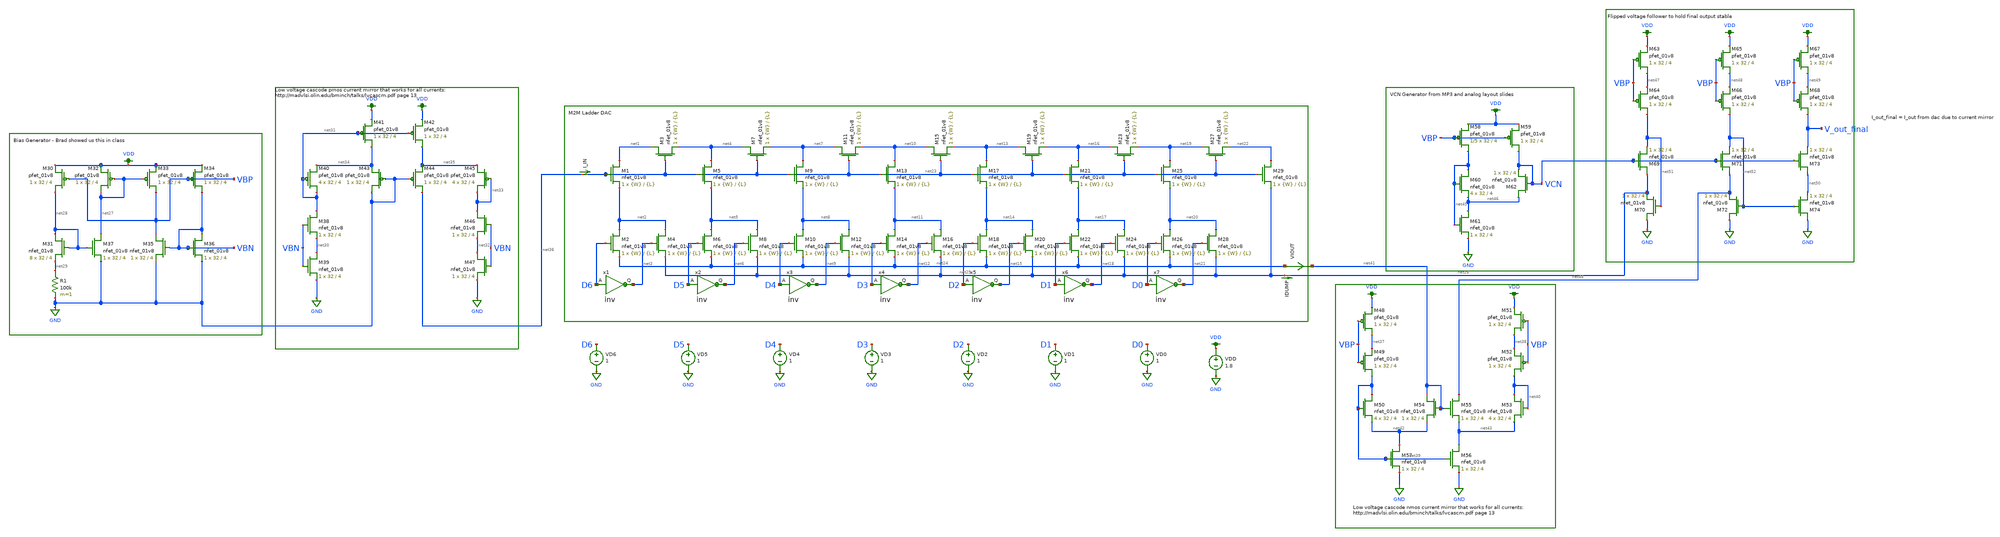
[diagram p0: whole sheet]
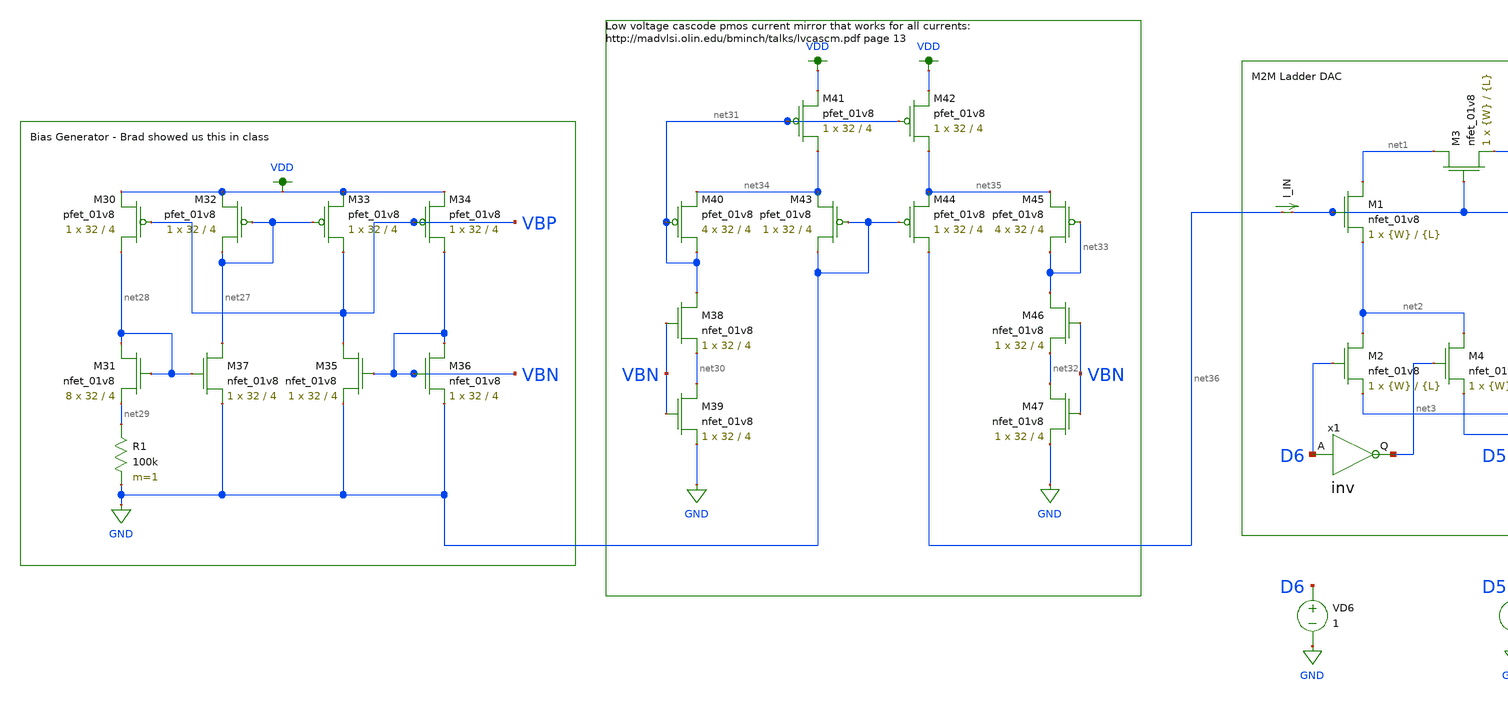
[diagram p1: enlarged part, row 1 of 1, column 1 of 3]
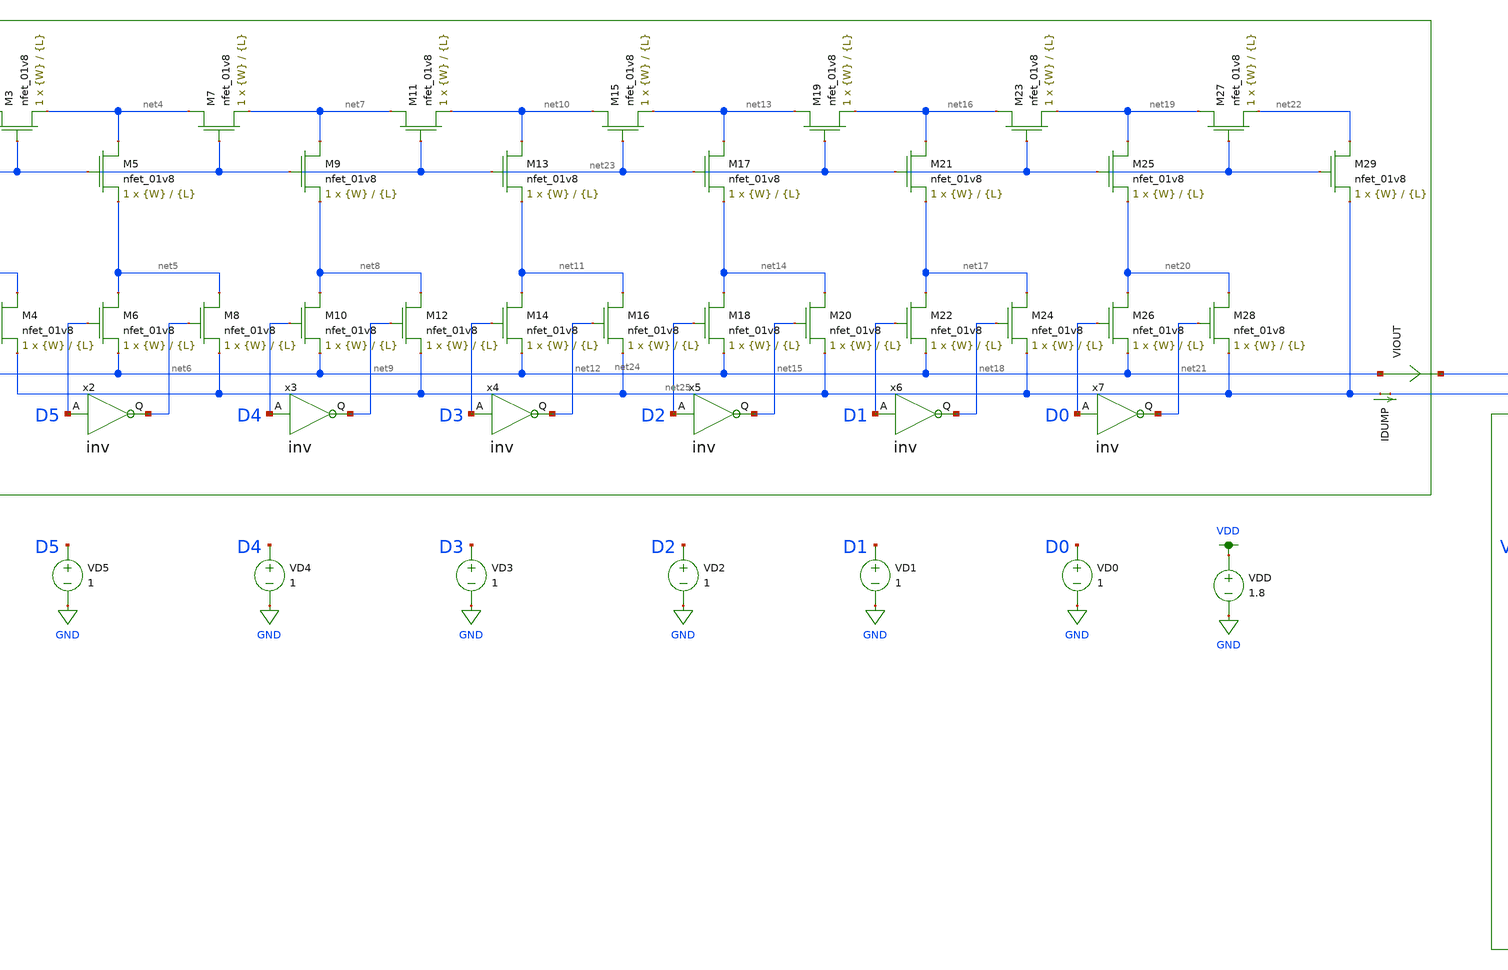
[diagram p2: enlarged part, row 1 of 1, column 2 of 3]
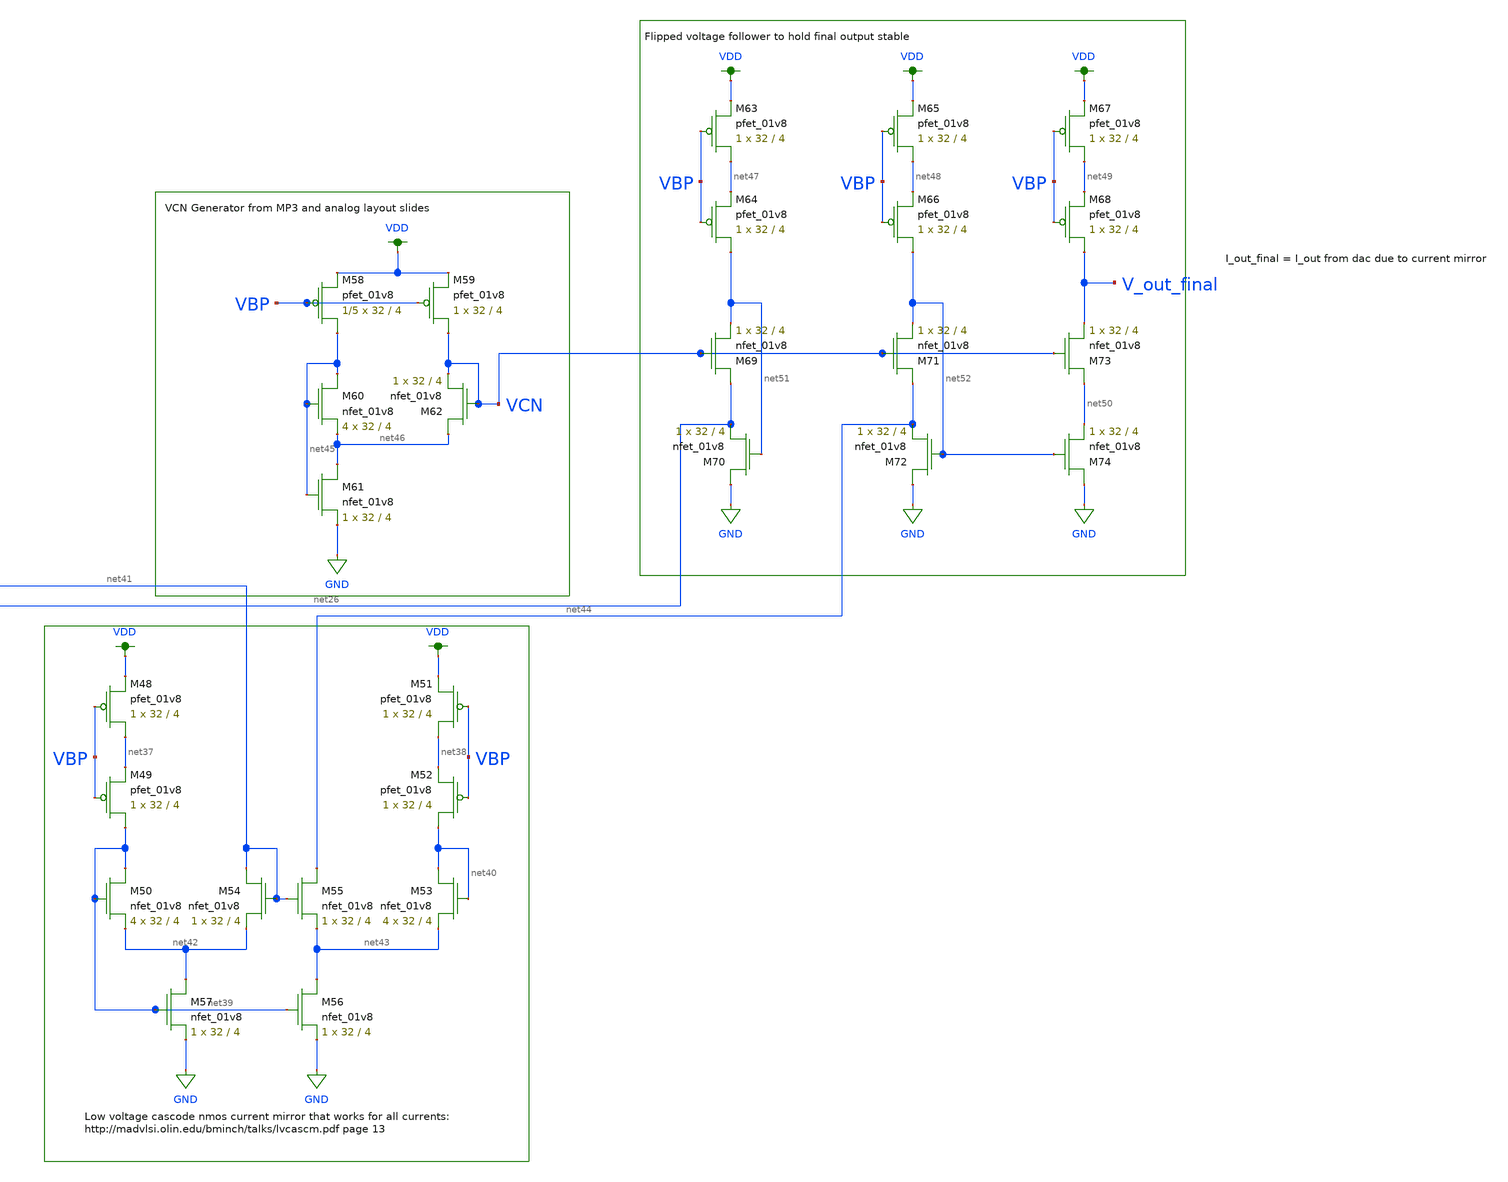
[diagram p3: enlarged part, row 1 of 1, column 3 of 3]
** sch_path: top_dac7.sch
**.subckt top_dac7
XM1 net1 net23 net2 GND sky130_fd_pr__nfet_01v8 L={L} W={W} nf=1 ad='int((nf+1)/2) * W/nf * 0.29' as='int((nf+2)/2) * W/nf * 0.29'
+ pd='2*int((nf+1)/2) * (W/nf + 0.29)' ps='2*int((nf+2)/2) * (W/nf + 0.29)' nrd='0.29 / W' nrs='0.29 / W'
+ sa=0 sb=0 sd=0 mult=1 m=1
XM2 net2 D6 net24 GND sky130_fd_pr__nfet_01v8 L={L} W={W} nf=1 ad='int((nf+1)/2) * W/nf * 0.29' as='int((nf+2)/2) * W/nf * 0.29'
+ pd='2*int((nf+1)/2) * (W/nf + 0.29)' ps='2*int((nf+2)/2) * (W/nf + 0.29)' nrd='0.29 / W' nrs='0.29 / W'
+ sa=0 sb=0 sd=0 mult=1 m=1
XM3 net1 net23 net4 GND sky130_fd_pr__nfet_01v8 L={L} W={W} nf=1 ad='int((nf+1)/2) * W/nf * 0.29' as='int((nf+2)/2) * W/nf * 0.29'
+ pd='2*int((nf+1)/2) * (W/nf + 0.29)' ps='2*int((nf+2)/2) * (W/nf + 0.29)' nrd='0.29 / W' nrs='0.29 / W'
+ sa=0 sb=0 sd=0 mult=1 m=1
XM4 net2 net3 net25 GND sky130_fd_pr__nfet_01v8 L={L} W={W} nf=1 ad='int((nf+1)/2) * W/nf * 0.29' as='int((nf+2)/2) * W/nf * 0.29'
+ pd='2*int((nf+1)/2) * (W/nf + 0.29)' ps='2*int((nf+2)/2) * (W/nf + 0.29)' nrd='0.29 / W' nrs='0.29 / W'
+ sa=0 sb=0 sd=0 mult=1 m=1
XM5 net4 net23 net5 GND sky130_fd_pr__nfet_01v8 L={L} W={W} nf=1 ad='int((nf+1)/2) * W/nf * 0.29' as='int((nf+2)/2) * W/nf * 0.29'
+ pd='2*int((nf+1)/2) * (W/nf + 0.29)' ps='2*int((nf+2)/2) * (W/nf + 0.29)' nrd='0.29 / W' nrs='0.29 / W'
+ sa=0 sb=0 sd=0 mult=1 m=1
XM6 net5 D5 net24 GND sky130_fd_pr__nfet_01v8 L={L} W={W} nf=1 ad='int((nf+1)/2) * W/nf * 0.29' as='int((nf+2)/2) * W/nf * 0.29'
+ pd='2*int((nf+1)/2) * (W/nf + 0.29)' ps='2*int((nf+2)/2) * (W/nf + 0.29)' nrd='0.29 / W' nrs='0.29 / W'
+ sa=0 sb=0 sd=0 mult=1 m=1
XM7 net4 net23 net7 GND sky130_fd_pr__nfet_01v8 L={L} W={W} nf=1 ad='int((nf+1)/2) * W/nf * 0.29' as='int((nf+2)/2) * W/nf * 0.29'
+ pd='2*int((nf+1)/2) * (W/nf + 0.29)' ps='2*int((nf+2)/2) * (W/nf + 0.29)' nrd='0.29 / W' nrs='0.29 / W'
+ sa=0 sb=0 sd=0 mult=1 m=1
XM8 net5 net6 net25 GND sky130_fd_pr__nfet_01v8 L={L} W={W} nf=1 ad='int((nf+1)/2) * W/nf * 0.29' as='int((nf+2)/2) * W/nf * 0.29'
+ pd='2*int((nf+1)/2) * (W/nf + 0.29)' ps='2*int((nf+2)/2) * (W/nf + 0.29)' nrd='0.29 / W' nrs='0.29 / W'
+ sa=0 sb=0 sd=0 mult=1 m=1
XM9 net7 net23 net8 GND sky130_fd_pr__nfet_01v8 L={L} W={W} nf=1 ad='int((nf+1)/2) * W/nf * 0.29' as='int((nf+2)/2) * W/nf * 0.29'
+ pd='2*int((nf+1)/2) * (W/nf + 0.29)' ps='2*int((nf+2)/2) * (W/nf + 0.29)' nrd='0.29 / W' nrs='0.29 / W'
+ sa=0 sb=0 sd=0 mult=1 m=1
XM10 net8 D4 net24 GND sky130_fd_pr__nfet_01v8 L={L} W={W} nf=1 ad='int((nf+1)/2) * W/nf * 0.29' as='int((nf+2)/2) * W/nf * 0.29'
+ pd='2*int((nf+1)/2) * (W/nf + 0.29)' ps='2*int((nf+2)/2) * (W/nf + 0.29)' nrd='0.29 / W' nrs='0.29 / W'
+ sa=0 sb=0 sd=0 mult=1 m=1
XM11 net7 net23 net10 GND sky130_fd_pr__nfet_01v8 L={L} W={W} nf=1 ad='int((nf+1)/2) * W/nf * 0.29' as='int((nf+2)/2) * W/nf * 0.29'
+ pd='2*int((nf+1)/2) * (W/nf + 0.29)' ps='2*int((nf+2)/2) * (W/nf + 0.29)' nrd='0.29 / W' nrs='0.29 / W'
+ sa=0 sb=0 sd=0 mult=1 m=1
XM12 net8 net9 net25 GND sky130_fd_pr__nfet_01v8 L={L} W={W} nf=1 ad='int((nf+1)/2) * W/nf * 0.29' as='int((nf+2)/2) * W/nf * 0.29'
+ pd='2*int((nf+1)/2) * (W/nf + 0.29)' ps='2*int((nf+2)/2) * (W/nf + 0.29)' nrd='0.29 / W' nrs='0.29 / W'
+ sa=0 sb=0 sd=0 mult=1 m=1
XM13 net10 net23 net11 GND sky130_fd_pr__nfet_01v8 L={L} W={W} nf=1 ad='int((nf+1)/2) * W/nf * 0.29'
+ as='int((nf+2)/2) * W/nf * 0.29' pd='2*int((nf+1)/2) * (W/nf + 0.29)' ps='2*int((nf+2)/2) * (W/nf + 0.29)'
+ nrd='0.29 / W' nrs='0.29 / W' sa=0 sb=0 sd=0 mult=1 m=1
XM14 net11 D3 net24 GND sky130_fd_pr__nfet_01v8 L={L} W={W} nf=1 ad='int((nf+1)/2) * W/nf * 0.29' as='int((nf+2)/2) * W/nf * 0.29'
+ pd='2*int((nf+1)/2) * (W/nf + 0.29)' ps='2*int((nf+2)/2) * (W/nf + 0.29)' nrd='0.29 / W' nrs='0.29 / W'
+ sa=0 sb=0 sd=0 mult=1 m=1
XM15 net10 net23 net13 GND sky130_fd_pr__nfet_01v8 L={L} W={W} nf=1 ad='int((nf+1)/2) * W/nf * 0.29'
+ as='int((nf+2)/2) * W/nf * 0.29' pd='2*int((nf+1)/2) * (W/nf + 0.29)' ps='2*int((nf+2)/2) * (W/nf + 0.29)'
+ nrd='0.29 / W' nrs='0.29 / W' sa=0 sb=0 sd=0 mult=1 m=1
XM16 net11 net12 net25 GND sky130_fd_pr__nfet_01v8 L={L} W={W} nf=1 ad='int((nf+1)/2) * W/nf * 0.29'
+ as='int((nf+2)/2) * W/nf * 0.29' pd='2*int((nf+1)/2) * (W/nf + 0.29)' ps='2*int((nf+2)/2) * (W/nf + 0.29)'
+ nrd='0.29 / W' nrs='0.29 / W' sa=0 sb=0 sd=0 mult=1 m=1
XM17 net13 net23 net14 GND sky130_fd_pr__nfet_01v8 L={L} W={W} nf=1 ad='int((nf+1)/2) * W/nf * 0.29'
+ as='int((nf+2)/2) * W/nf * 0.29' pd='2*int((nf+1)/2) * (W/nf + 0.29)' ps='2*int((nf+2)/2) * (W/nf + 0.29)'
+ nrd='0.29 / W' nrs='0.29 / W' sa=0 sb=0 sd=0 mult=1 m=1
XM18 net14 D2 net24 GND sky130_fd_pr__nfet_01v8 L={L} W={W} nf=1 ad='int((nf+1)/2) * W/nf * 0.29' as='int((nf+2)/2) * W/nf * 0.29'
+ pd='2*int((nf+1)/2) * (W/nf + 0.29)' ps='2*int((nf+2)/2) * (W/nf + 0.29)' nrd='0.29 / W' nrs='0.29 / W'
+ sa=0 sb=0 sd=0 mult=1 m=1
XM19 net13 net23 net16 GND sky130_fd_pr__nfet_01v8 L={L} W={W} nf=1 ad='int((nf+1)/2) * W/nf * 0.29'
+ as='int((nf+2)/2) * W/nf * 0.29' pd='2*int((nf+1)/2) * (W/nf + 0.29)' ps='2*int((nf+2)/2) * (W/nf + 0.29)'
+ nrd='0.29 / W' nrs='0.29 / W' sa=0 sb=0 sd=0 mult=1 m=1
XM20 net14 net15 net25 GND sky130_fd_pr__nfet_01v8 L={L} W={W} nf=1 ad='int((nf+1)/2) * W/nf * 0.29'
+ as='int((nf+2)/2) * W/nf * 0.29' pd='2*int((nf+1)/2) * (W/nf + 0.29)' ps='2*int((nf+2)/2) * (W/nf + 0.29)'
+ nrd='0.29 / W' nrs='0.29 / W' sa=0 sb=0 sd=0 mult=1 m=1
XM21 net16 net23 net17 GND sky130_fd_pr__nfet_01v8 L={L} W={W} nf=1 ad='int((nf+1)/2) * W/nf * 0.29'
+ as='int((nf+2)/2) * W/nf * 0.29' pd='2*int((nf+1)/2) * (W/nf + 0.29)' ps='2*int((nf+2)/2) * (W/nf + 0.29)'
+ nrd='0.29 / W' nrs='0.29 / W' sa=0 sb=0 sd=0 mult=1 m=1
XM22 net17 D1 net24 GND sky130_fd_pr__nfet_01v8 L={L} W={W} nf=1 ad='int((nf+1)/2) * W/nf * 0.29' as='int((nf+2)/2) * W/nf * 0.29'
+ pd='2*int((nf+1)/2) * (W/nf + 0.29)' ps='2*int((nf+2)/2) * (W/nf + 0.29)' nrd='0.29 / W' nrs='0.29 / W'
+ sa=0 sb=0 sd=0 mult=1 m=1
XM23 net16 net23 net19 GND sky130_fd_pr__nfet_01v8 L={L} W={W} nf=1 ad='int((nf+1)/2) * W/nf * 0.29'
+ as='int((nf+2)/2) * W/nf * 0.29' pd='2*int((nf+1)/2) * (W/nf + 0.29)' ps='2*int((nf+2)/2) * (W/nf + 0.29)'
+ nrd='0.29 / W' nrs='0.29 / W' sa=0 sb=0 sd=0 mult=1 m=1
XM24 net17 net18 net25 GND sky130_fd_pr__nfet_01v8 L={L} W={W} nf=1 ad='int((nf+1)/2) * W/nf * 0.29'
+ as='int((nf+2)/2) * W/nf * 0.29' pd='2*int((nf+1)/2) * (W/nf + 0.29)' ps='2*int((nf+2)/2) * (W/nf + 0.29)'
+ nrd='0.29 / W' nrs='0.29 / W' sa=0 sb=0 sd=0 mult=1 m=1
XM25 net19 net23 net20 GND sky130_fd_pr__nfet_01v8 L={L} W={W} nf=1 ad='int((nf+1)/2) * W/nf * 0.29'
+ as='int((nf+2)/2) * W/nf * 0.29' pd='2*int((nf+1)/2) * (W/nf + 0.29)' ps='2*int((nf+2)/2) * (W/nf + 0.29)'
+ nrd='0.29 / W' nrs='0.29 / W' sa=0 sb=0 sd=0 mult=1 m=1
XM26 net20 D0 net24 GND sky130_fd_pr__nfet_01v8 L={L} W={W} nf=1 ad='int((nf+1)/2) * W/nf * 0.29' as='int((nf+2)/2) * W/nf * 0.29'
+ pd='2*int((nf+1)/2) * (W/nf + 0.29)' ps='2*int((nf+2)/2) * (W/nf + 0.29)' nrd='0.29 / W' nrs='0.29 / W'
+ sa=0 sb=0 sd=0 mult=1 m=1
XM27 net19 net23 net22 GND sky130_fd_pr__nfet_01v8 L={L} W={W} nf=1 ad='int((nf+1)/2) * W/nf * 0.29'
+ as='int((nf+2)/2) * W/nf * 0.29' pd='2*int((nf+1)/2) * (W/nf + 0.29)' ps='2*int((nf+2)/2) * (W/nf + 0.29)'
+ nrd='0.29 / W' nrs='0.29 / W' sa=0 sb=0 sd=0 mult=1 m=1
XM28 net20 net21 net25 GND sky130_fd_pr__nfet_01v8 L={L} W={W} nf=1 ad='int((nf+1)/2) * W/nf * 0.29'
+ as='int((nf+2)/2) * W/nf * 0.29' pd='2*int((nf+1)/2) * (W/nf + 0.29)' ps='2*int((nf+2)/2) * (W/nf + 0.29)'
+ nrd='0.29 / W' nrs='0.29 / W' sa=0 sb=0 sd=0 mult=1 m=1
XM29 net22 net23 net25 GND sky130_fd_pr__nfet_01v8 L={L} W={W} nf=1 ad='int((nf+1)/2) * W/nf * 0.29'
+ as='int((nf+2)/2) * W/nf * 0.29' pd='2*int((nf+1)/2) * (W/nf + 0.29)' ps='2*int((nf+2)/2) * (W/nf + 0.29)'
+ nrd='0.29 / W' nrs='0.29 / W' sa=0 sb=0 sd=0 mult=1 m=1
IDUMP net25 net26 0
.save i(idump)
I_IN net36 net23 0
.save i(i_in)
x1 net3 D6 inv
x2 net6 D5 inv
x3 net9 D4 inv
x4 net12 D3 inv
x5 net15 D2 inv
x6 net18 D1 inv
x7 net21 D0 inv
XM30 net28 VBP VDD VDD sky130_fd_pr__pfet_01v8 L=4 W=32 nf=1 ad='int((nf+1)/2) * W/nf * 0.29' as='int((nf+2)/2) * W/nf * 0.29'
+ pd='2*int((nf+1)/2) * (W/nf + 0.29)' ps='2*int((nf+2)/2) * (W/nf + 0.29)' nrd='0.29 / W' nrs='0.29 / W'
+ sa=0 sb=0 sd=0 mult=1 m=1
XM31 net28 net28 net29 GND sky130_fd_pr__nfet_01v8 L=4 W=32 nf=1 ad='int((nf+1)/2) * W/nf * 0.29' as='int((nf+2)/2) * W/nf * 0.29'
+ pd='2*int((nf+1)/2) * (W/nf + 0.29)' ps='2*int((nf+2)/2) * (W/nf + 0.29)' nrd='0.29 / W' nrs='0.29 / W'
+ sa=0 sb=0 sd=0 mult=8 m=8
XM32 net27 net27 VDD VDD sky130_fd_pr__pfet_01v8 L=4 W=32 nf=1 ad='int((nf+1)/2) * W/nf * 0.29' as='int((nf+2)/2) * W/nf * 0.29'
+ pd='2*int((nf+1)/2) * (W/nf + 0.29)' ps='2*int((nf+2)/2) * (W/nf + 0.29)' nrd='0.29 / W' nrs='0.29 / W'
+ sa=0 sb=0 sd=0 mult=1 m=1
XM33 VBP net27 VDD VDD sky130_fd_pr__pfet_01v8 L=4 W=32 nf=1 ad='int((nf+1)/2) * W/nf * 0.29' as='int((nf+2)/2) * W/nf * 0.29'
+ pd='2*int((nf+1)/2) * (W/nf + 0.29)' ps='2*int((nf+2)/2) * (W/nf + 0.29)' nrd='0.29 / W' nrs='0.29 / W'
+ sa=0 sb=0 sd=0 mult=1 m=1
XM34 VBN VBP VDD VDD sky130_fd_pr__pfet_01v8 L=4 W=32 nf=1 ad='int((nf+1)/2) * W/nf * 0.29' as='int((nf+2)/2) * W/nf * 0.29'
+ pd='2*int((nf+1)/2) * (W/nf + 0.29)' ps='2*int((nf+2)/2) * (W/nf + 0.29)' nrd='0.29 / W' nrs='0.29 / W'
+ sa=0 sb=0 sd=0 mult=1 m=1
XM35 VBP VBN GND GND sky130_fd_pr__nfet_01v8 L=4 W=32 nf=1 ad='int((nf+1)/2) * W/nf * 0.29' as='int((nf+2)/2) * W/nf * 0.29'
+ pd='2*int((nf+1)/2) * (W/nf + 0.29)' ps='2*int((nf+2)/2) * (W/nf + 0.29)' nrd='0.29 / W' nrs='0.29 / W'
+ sa=0 sb=0 sd=0 mult=1 m=1
XM36 VBN VBN GND GND sky130_fd_pr__nfet_01v8 L=4 W=32 nf=1 ad='int((nf+1)/2) * W/nf * 0.29' as='int((nf+2)/2) * W/nf * 0.29'
+ pd='2*int((nf+1)/2) * (W/nf + 0.29)' ps='2*int((nf+2)/2) * (W/nf + 0.29)' nrd='0.29 / W' nrs='0.29 / W'
+ sa=0 sb=0 sd=0 mult=1 m=1
XM37 net27 net28 GND GND sky130_fd_pr__nfet_01v8 L=4 W=32 nf=1 ad='int((nf+1)/2) * W/nf * 0.29' as='int((nf+2)/2) * W/nf * 0.29'
+ pd='2*int((nf+1)/2) * (W/nf + 0.29)' ps='2*int((nf+2)/2) * (W/nf + 0.29)' nrd='0.29 / W' nrs='0.29 / W'
+ sa=0 sb=0 sd=0 mult=1 m=1
R1 net29 GND 100k m=1
XM38 net31 VBN net30 GND sky130_fd_pr__nfet_01v8 L=4 W=32 nf=1 ad='int((nf+1)/2) * W/nf * 0.29' as='int((nf+2)/2) * W/nf * 0.29'
+ pd='2*int((nf+1)/2) * (W/nf + 0.29)' ps='2*int((nf+2)/2) * (W/nf + 0.29)' nrd='0.29 / W' nrs='0.29 / W'
+ sa=0 sb=0 sd=0 mult=1 m=1
XM39 net30 VBN GND GND sky130_fd_pr__nfet_01v8 L=4 W=32 nf=1 ad='int((nf+1)/2) * W/nf * 0.29' as='int((nf+2)/2) * W/nf * 0.29'
+ pd='2*int((nf+1)/2) * (W/nf + 0.29)' ps='2*int((nf+2)/2) * (W/nf + 0.29)' nrd='0.29 / W' nrs='0.29 / W'
+ sa=0 sb=0 sd=0 mult=1 m=1
XM40 net31 net31 net34 VDD sky130_fd_pr__pfet_01v8 L=4 W=32 nf=1 ad='int((nf+1)/2) * W/nf * 0.29' as='int((nf+2)/2) * W/nf * 0.29'
+ pd='2*int((nf+1)/2) * (W/nf + 0.29)' ps='2*int((nf+2)/2) * (W/nf + 0.29)' nrd='0.29 / W' nrs='0.29 / W'
+ sa=0 sb=0 sd=0 mult=4 m=4
XM41 net34 net31 VDD VDD sky130_fd_pr__pfet_01v8 L=4 W=32 nf=1 ad='int((nf+1)/2) * W/nf * 0.29' as='int((nf+2)/2) * W/nf * 0.29'
+ pd='2*int((nf+1)/2) * (W/nf + 0.29)' ps='2*int((nf+2)/2) * (W/nf + 0.29)' nrd='0.29 / W' nrs='0.29 / W'
+ sa=0 sb=0 sd=0 mult=1 m=1
XM42 net35 net31 VDD VDD sky130_fd_pr__pfet_01v8 L=4 W=32 nf=1 ad='int((nf+1)/2) * W/nf * 0.29' as='int((nf+2)/2) * W/nf * 0.29'
+ pd='2*int((nf+1)/2) * (W/nf + 0.29)' ps='2*int((nf+2)/2) * (W/nf + 0.29)' nrd='0.29 / W' nrs='0.29 / W'
+ sa=0 sb=0 sd=0 mult=1 m=1
XM43 GND GND net34 VDD sky130_fd_pr__pfet_01v8 L=4 W=32 nf=1 ad='int((nf+1)/2) * W/nf * 0.29' as='int((nf+2)/2) * W/nf * 0.29'
+ pd='2*int((nf+1)/2) * (W/nf + 0.29)' ps='2*int((nf+2)/2) * (W/nf + 0.29)' nrd='0.29 / W' nrs='0.29 / W'
+ sa=0 sb=0 sd=0 mult=1 m=1
XM44 net36 GND net35 VDD sky130_fd_pr__pfet_01v8 L=4 W=32 nf=1 ad='int((nf+1)/2) * W/nf * 0.29' as='int((nf+2)/2) * W/nf * 0.29'
+ pd='2*int((nf+1)/2) * (W/nf + 0.29)' ps='2*int((nf+2)/2) * (W/nf + 0.29)' nrd='0.29 / W' nrs='0.29 / W'
+ sa=0 sb=0 sd=0 mult=1 m=1
XM45 net33 net33 net35 VDD sky130_fd_pr__pfet_01v8 L=4 W=32 nf=1 ad='int((nf+1)/2) * W/nf * 0.29' as='int((nf+2)/2) * W/nf * 0.29'
+ pd='2*int((nf+1)/2) * (W/nf + 0.29)' ps='2*int((nf+2)/2) * (W/nf + 0.29)' nrd='0.29 / W' nrs='0.29 / W'
+ sa=0 sb=0 sd=0 mult=4 m=4
XM46 net33 VBN net32 GND sky130_fd_pr__nfet_01v8 L=4 W=32 nf=1 ad='int((nf+1)/2) * W/nf * 0.29' as='int((nf+2)/2) * W/nf * 0.29'
+ pd='2*int((nf+1)/2) * (W/nf + 0.29)' ps='2*int((nf+2)/2) * (W/nf + 0.29)' nrd='0.29 / W' nrs='0.29 / W'
+ sa=0 sb=0 sd=0 mult=1 m=1
XM47 net32 VBN GND GND sky130_fd_pr__nfet_01v8 L=4 W=32 nf=1 ad='int((nf+1)/2) * W/nf * 0.29' as='int((nf+2)/2) * W/nf * 0.29'
+ pd='2*int((nf+1)/2) * (W/nf + 0.29)' ps='2*int((nf+2)/2) * (W/nf + 0.29)' nrd='0.29 / W' nrs='0.29 / W'
+ sa=0 sb=0 sd=0 mult=1 m=1
XM48 net37 VBP VDD VDD sky130_fd_pr__pfet_01v8 L=4 W=32 nf=1 ad='int((nf+1)/2) * W/nf * 0.29' as='int((nf+2)/2) * W/nf * 0.29'
+ pd='2*int((nf+1)/2) * (W/nf + 0.29)' ps='2*int((nf+2)/2) * (W/nf + 0.29)' nrd='0.29 / W' nrs='0.29 / W'
+ sa=0 sb=0 sd=0 mult=1 m=1
XM49 net39 VBP net37 VDD sky130_fd_pr__pfet_01v8 L=4 W=32 nf=1 ad='int((nf+1)/2) * W/nf * 0.29' as='int((nf+2)/2) * W/nf * 0.29'
+ pd='2*int((nf+1)/2) * (W/nf + 0.29)' ps='2*int((nf+2)/2) * (W/nf + 0.29)' nrd='0.29 / W' nrs='0.29 / W'
+ sa=0 sb=0 sd=0 mult=1 m=1
XM50 net39 net39 net42 GND sky130_fd_pr__nfet_01v8 L=4 W=32 nf=1 ad='int((nf+1)/2) * W/nf * 0.29' as='int((nf+2)/2) * W/nf * 0.29'
+ pd='2*int((nf+1)/2) * (W/nf + 0.29)' ps='2*int((nf+2)/2) * (W/nf + 0.29)' nrd='0.29 / W' nrs='0.29 / W'
+ sa=0 sb=0 sd=0 mult=4 m=4
XM51 net38 VBP VDD VDD sky130_fd_pr__pfet_01v8 L=4 W=32 nf=1 ad='int((nf+1)/2) * W/nf * 0.29' as='int((nf+2)/2) * W/nf * 0.29'
+ pd='2*int((nf+1)/2) * (W/nf + 0.29)' ps='2*int((nf+2)/2) * (W/nf + 0.29)' nrd='0.29 / W' nrs='0.29 / W'
+ sa=0 sb=0 sd=0 mult=1 m=1
XM52 net40 VBP net38 VDD sky130_fd_pr__pfet_01v8 L=4 W=32 nf=1 ad='int((nf+1)/2) * W/nf * 0.29' as='int((nf+2)/2) * W/nf * 0.29'
+ pd='2*int((nf+1)/2) * (W/nf + 0.29)' ps='2*int((nf+2)/2) * (W/nf + 0.29)' nrd='0.29 / W' nrs='0.29 / W'
+ sa=0 sb=0 sd=0 mult=1 m=1
XM53 net40 net40 net43 GND sky130_fd_pr__nfet_01v8 L=4 W=32 nf=1 ad='int((nf+1)/2) * W/nf * 0.29' as='int((nf+2)/2) * W/nf * 0.29'
+ pd='2*int((nf+1)/2) * (W/nf + 0.29)' ps='2*int((nf+2)/2) * (W/nf + 0.29)' nrd='0.29 / W' nrs='0.29 / W'
+ sa=0 sb=0 sd=0 mult=4 m=4
XM54 net41 net41 net42 GND sky130_fd_pr__nfet_01v8 L=4 W=32 nf=1 ad='int((nf+1)/2) * W/nf * 0.29' as='int((nf+2)/2) * W/nf * 0.29'
+ pd='2*int((nf+1)/2) * (W/nf + 0.29)' ps='2*int((nf+2)/2) * (W/nf + 0.29)' nrd='0.29 / W' nrs='0.29 / W'
+ sa=0 sb=0 sd=0 mult=1 m=1
XM55 net44 net41 net43 GND sky130_fd_pr__nfet_01v8 L=4 W=32 nf=1 ad='int((nf+1)/2) * W/nf * 0.29' as='int((nf+2)/2) * W/nf * 0.29'
+ pd='2*int((nf+1)/2) * (W/nf + 0.29)' ps='2*int((nf+2)/2) * (W/nf + 0.29)' nrd='0.29 / W' nrs='0.29 / W'
+ sa=0 sb=0 sd=0 mult=1 m=1
XM56 net43 net39 GND GND sky130_fd_pr__nfet_01v8 L=4 W=32 nf=1 ad='int((nf+1)/2) * W/nf * 0.29' as='int((nf+2)/2) * W/nf * 0.29'
+ pd='2*int((nf+1)/2) * (W/nf + 0.29)' ps='2*int((nf+2)/2) * (W/nf + 0.29)' nrd='0.29 / W' nrs='0.29 / W'
+ sa=0 sb=0 sd=0 mult=1 m=1
XM57 net42 net39 GND GND sky130_fd_pr__nfet_01v8 L=4 W=32 nf=1 ad='int((nf+1)/2) * W/nf * 0.29' as='int((nf+2)/2) * W/nf * 0.29'
+ pd='2*int((nf+1)/2) * (W/nf + 0.29)' ps='2*int((nf+2)/2) * (W/nf + 0.29)' nrd='0.29 / W' nrs='0.29 / W'
+ sa=0 sb=0 sd=0 mult=1 m=1
XM58 net45 VBP VDD VDD sky130_fd_pr__pfet_01v8 L=4 W=32 nf=1 ad='int((nf+1)/2) * W/nf * 0.29' as='int((nf+2)/2) * W/nf * 0.29'
+ pd='2*int((nf+1)/2) * (W/nf + 0.29)' ps='2*int((nf+2)/2) * (W/nf + 0.29)' nrd='0.29 / W' nrs='0.29 / W'
+ sa=0 sb=0 sd=0 mult=1/5 m=1/5
XM59 VCN VBP VDD VDD sky130_fd_pr__pfet_01v8 L=4 W=32 nf=1 ad='int((nf+1)/2) * W/nf * 0.29' as='int((nf+2)/2) * W/nf * 0.29'
+ pd='2*int((nf+1)/2) * (W/nf + 0.29)' ps='2*int((nf+2)/2) * (W/nf + 0.29)' nrd='0.29 / W' nrs='0.29 / W'
+ sa=0 sb=0 sd=0 mult=1 m=1
XM60 net45 net45 net46 GND sky130_fd_pr__nfet_01v8 L=4 W=32 nf=1 ad='int((nf+1)/2) * W/nf * 0.29' as='int((nf+2)/2) * W/nf * 0.29'
+ pd='2*int((nf+1)/2) * (W/nf + 0.29)' ps='2*int((nf+2)/2) * (W/nf + 0.29)' nrd='0.29 / W' nrs='0.29 / W'
+ sa=0 sb=0 sd=0 mult=4 m=4
XM61 net46 net45 GND GND sky130_fd_pr__nfet_01v8 L=4 W=32 nf=1 ad='int((nf+1)/2) * W/nf * 0.29' as='int((nf+2)/2) * W/nf * 0.29'
+ pd='2*int((nf+1)/2) * (W/nf + 0.29)' ps='2*int((nf+2)/2) * (W/nf + 0.29)' nrd='0.29 / W' nrs='0.29 / W'
+ sa=0 sb=0 sd=0 mult=1 m=1
XM62 net46 VCN VCN GND sky130_fd_pr__nfet_01v8 L=4 W=32 nf=1 ad='int((nf+1)/2) * W/nf * 0.29' as='int((nf+2)/2) * W/nf * 0.29'
+ pd='2*int((nf+1)/2) * (W/nf + 0.29)' ps='2*int((nf+2)/2) * (W/nf + 0.29)' nrd='0.29 / W' nrs='0.29 / W'
+ sa=0 sb=0 sd=0 mult=1 m=1
XM63 net47 VBP VDD VDD sky130_fd_pr__pfet_01v8 L=4 W=32 nf=1 ad='int((nf+1)/2) * W/nf * 0.29' as='int((nf+2)/2) * W/nf * 0.29'
+ pd='2*int((nf+1)/2) * (W/nf + 0.29)' ps='2*int((nf+2)/2) * (W/nf + 0.29)' nrd='0.29 / W' nrs='0.29 / W'
+ sa=0 sb=0 sd=0 mult=1 m=1
XM64 net51 VBP net47 VDD sky130_fd_pr__pfet_01v8 L=4 W=32 nf=1 ad='int((nf+1)/2) * W/nf * 0.29' as='int((nf+2)/2) * W/nf * 0.29'
+ pd='2*int((nf+1)/2) * (W/nf + 0.29)' ps='2*int((nf+2)/2) * (W/nf + 0.29)' nrd='0.29 / W' nrs='0.29 / W'
+ sa=0 sb=0 sd=0 mult=1 m=1
XM65 net48 VBP VDD VDD sky130_fd_pr__pfet_01v8 L=4 W=32 nf=1 ad='int((nf+1)/2) * W/nf * 0.29' as='int((nf+2)/2) * W/nf * 0.29'
+ pd='2*int((nf+1)/2) * (W/nf + 0.29)' ps='2*int((nf+2)/2) * (W/nf + 0.29)' nrd='0.29 / W' nrs='0.29 / W'
+ sa=0 sb=0 sd=0 mult=1 m=1
XM66 net52 VBP net48 VDD sky130_fd_pr__pfet_01v8 L=4 W=32 nf=1 ad='int((nf+1)/2) * W/nf * 0.29' as='int((nf+2)/2) * W/nf * 0.29'
+ pd='2*int((nf+1)/2) * (W/nf + 0.29)' ps='2*int((nf+2)/2) * (W/nf + 0.29)' nrd='0.29 / W' nrs='0.29 / W'
+ sa=0 sb=0 sd=0 mult=1 m=1
XM67 net49 VBP VDD VDD sky130_fd_pr__pfet_01v8 L=4 W=32 nf=1 ad='int((nf+1)/2) * W/nf * 0.29' as='int((nf+2)/2) * W/nf * 0.29'
+ pd='2*int((nf+1)/2) * (W/nf + 0.29)' ps='2*int((nf+2)/2) * (W/nf + 0.29)' nrd='0.29 / W' nrs='0.29 / W'
+ sa=0 sb=0 sd=0 mult=1 m=1
XM68 V_out_final VBP net49 VDD sky130_fd_pr__pfet_01v8 L=4 W=32 nf=1 ad='int((nf+1)/2) * W/nf * 0.29'
+ as='int((nf+2)/2) * W/nf * 0.29' pd='2*int((nf+1)/2) * (W/nf + 0.29)' ps='2*int((nf+2)/2) * (W/nf + 0.29)'
+ nrd='0.29 / W' nrs='0.29 / W' sa=0 sb=0 sd=0 mult=1 m=1
XM69 net26 VCN net51 GND sky130_fd_pr__nfet_01v8 L=4 W=32 nf=1 ad='int((nf+1)/2) * W/nf * 0.29' as='int((nf+2)/2) * W/nf * 0.29'
+ pd='2*int((nf+1)/2) * (W/nf + 0.29)' ps='2*int((nf+2)/2) * (W/nf + 0.29)' nrd='0.29 / W' nrs='0.29 / W'
+ sa=0 sb=0 sd=0 mult=1 m=1
XM70 GND net51 net26 GND sky130_fd_pr__nfet_01v8 L=4 W=32 nf=1 ad='int((nf+1)/2) * W/nf * 0.29' as='int((nf+2)/2) * W/nf * 0.29'
+ pd='2*int((nf+1)/2) * (W/nf + 0.29)' ps='2*int((nf+2)/2) * (W/nf + 0.29)' nrd='0.29 / W' nrs='0.29 / W'
+ sa=0 sb=0 sd=0 mult=1 m=1
XM71 net44 VCN net52 GND sky130_fd_pr__nfet_01v8 L=4 W=32 nf=1 ad='int((nf+1)/2) * W/nf * 0.29' as='int((nf+2)/2) * W/nf * 0.29'
+ pd='2*int((nf+1)/2) * (W/nf + 0.29)' ps='2*int((nf+2)/2) * (W/nf + 0.29)' nrd='0.29 / W' nrs='0.29 / W'
+ sa=0 sb=0 sd=0 mult=1 m=1
XM72 GND net52 net44 GND sky130_fd_pr__nfet_01v8 L=4 W=32 nf=1 ad='int((nf+1)/2) * W/nf * 0.29' as='int((nf+2)/2) * W/nf * 0.29'
+ pd='2*int((nf+1)/2) * (W/nf + 0.29)' ps='2*int((nf+2)/2) * (W/nf + 0.29)' nrd='0.29 / W' nrs='0.29 / W'
+ sa=0 sb=0 sd=0 mult=1 m=1
XM73 net50 VCN V_out_final GND sky130_fd_pr__nfet_01v8 L=4 W=32 nf=1 ad='int((nf+1)/2) * W/nf * 0.29'
+ as='int((nf+2)/2) * W/nf * 0.29' pd='2*int((nf+1)/2) * (W/nf + 0.29)' ps='2*int((nf+2)/2) * (W/nf + 0.29)'
+ nrd='0.29 / W' nrs='0.29 / W' sa=0 sb=0 sd=0 mult=1 m=1
XM74 GND net52 net50 GND sky130_fd_pr__nfet_01v8 L=4 W=32 nf=1 ad='int((nf+1)/2) * W/nf * 0.29' as='int((nf+2)/2) * W/nf * 0.29'
+ pd='2*int((nf+1)/2) * (W/nf + 0.29)' ps='2*int((nf+2)/2) * (W/nf + 0.29)' nrd='0.29 / W' nrs='0.29 / W'
+ sa=0 sb=0 sd=0 mult=1 m=1
VDD VDD GND 1.8
VD6 D6 GND 1
VD1 D1 GND 1
VD2 D2 GND 1
VD3 D3 GND 1
VD4 D4 GND 1
VD5 D5 GND 1
VD0 D0 GND 1
VIOUT net24 net41 0
.save i(viout)
**** begin user architecture code

.option wnflag=1
.param MC_SWITCH=0.0
.lib ~/skywater/skywater-pdk/libraries/sky130_fd_pr_ngspice/latest/models/sky130.lib.spice tt


.param W=32 .param L=4
.control
    set wr_singlescale
    let runs = 1
    let run = 1
    while run <= runs
        set appendwrite = FALSE
        set wr_vecnames
        let code = 0
        while code < 128
            if code eq 0
                let D0 = 0
            else
                let D0 = code % 2
            end
            if floor(code / 2 ) eq 0
                let D1 = 0
            else
                let D1 = floor(code / 2 ) % 2
            end
            if floor(code / 4 ) eq 0
                let D2 = 0
            else
                let D2 = floor(code / 4 ) % 2
            end
            if floor(code / 8 ) eq 0
                let D3 = 0
            else
                let D3 = floor(code / 8 ) % 2
            end
            if floor(code / 16 ) eq 0
                let D4 = 0
            else
                let D4 = floor(code / 16 ) % 2
            end
            if floor(code / 32 ) eq 0
                let D5 = 0
            else
                let D5 = floor(code / 32 ) % 2
            end
            if floor(code / 64 ) eq 0
                let D6 = 0
            else
                let D6 = floor(code / 64) % 2
            end
            alter VD0 $&D0
            alter VD1 $&D1
            alter VD2 $&D2
            alter VD3 $&D3
            alter VD4 $&D4
            alter VD5 $&D5
            alter VD6 $&D6
            save all
            op
            wrdata ~/Documents/data_fld/MCDACDATA{$&run}.txt v(D0) v(D1) v(D2) v(D3) v(D4) v(D5) v(D6)
+ i(VIOUT) v(V_out_final)
            if code eq 0
                set appendwrite
                set wr_vecnames = FALSE
            end
            let code = code + 1
        end
        reset
        let run = run + 1
    end
    quit
.endc

**** end user architecture code
**.ends

* expanding   symbol:  /home/mstopyra/Documents/MADVLSI-MP4-DAC/schemas/inv.sym # of pins=2
** sym_path: /home/mstopyra/Documents/MADVLSI-MP4-DAC/schemas/inv.sym
** sch_path: /home/mstopyra/Documents/MADVLSI-MP4-DAC/schemas/inv.sch
.subckt inv Q A
*.ipin A
*.opin Q
XM1 Q A GND GND sky130_fd_pr__nfet_01v8 L=4 W=32 nf=1 ad='int((nf+1)/2) * W/nf * 0.29' as='int((nf+2)/2) * W/nf * 0.29'
+ pd='2*int((nf+1)/2) * (W/nf + 0.29)' ps='2*int((nf+2)/2) * (W/nf + 0.29)' nrd='0.29 / W' nrs='0.29 / W'
+ sa=0 sb=0 sd=0 mult=2 m=2
XM2 Q A VDD VDD sky130_fd_pr__pfet_01v8 L=4 W=32 nf=1 ad='int((nf+1)/2) * W/nf * 0.29' as='int((nf+2)/2) * W/nf * 0.29'
+ pd='2*int((nf+1)/2) * (W/nf + 0.29)' ps='2*int((nf+2)/2) * (W/nf + 0.29)' nrd='0.29 / W' nrs='0.29 / W'
+ sa=0 sb=0 sd=0 mult=1 m=1
.ends

.GLOBAL GND
.GLOBAL VDD
.end
